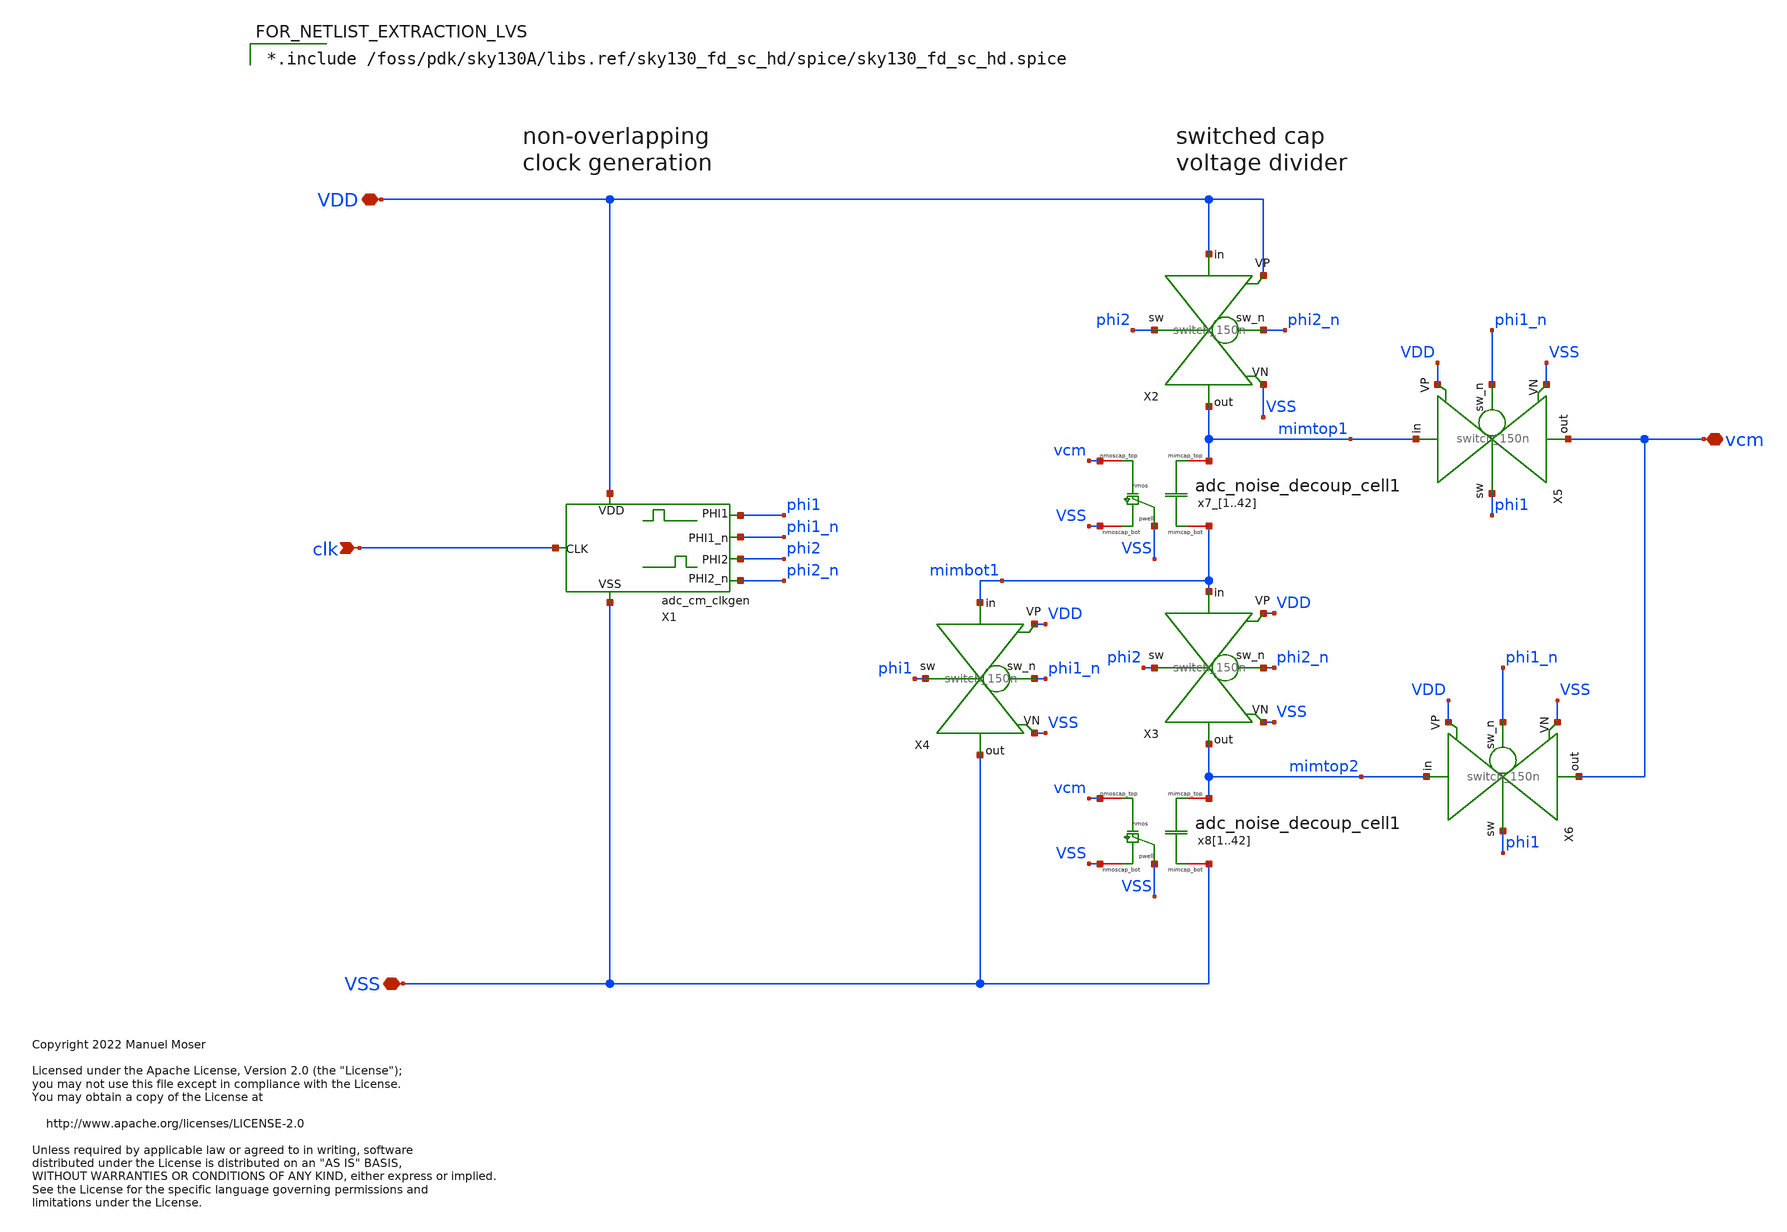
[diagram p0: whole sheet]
** sch_path: xschem/adc_vcm_gen/adc_vcm_gen.sch
* Copyright 2022 Manuel Moser
* Licensed under the Apache License, Version 2.0 (the "License");
**.subckt adc_vcm_gen VDD VSS clk vcm
*.iopin VDD
*.iopin VSS
*.ipin clk
*.iopin vcm
X1 clk VDD VSS phi1_n phi1 phi2 phi2_n adc_cm_clkgen
X2 phi2_n VDD phi2 mimtop1 VDD VSS switch_150n
X3 phi2_n mimbot1 phi2 mimtop2 VDD VSS switch_150n
X4 phi1_n mimbot1 phi1 VSS VDD VSS switch_150n
X5 phi1_n mimtop1 phi1 vcm VDD VSS switch_150n
X6 phi1_n mimtop2 phi1 vcm VDD VSS switch_150n
x7_1 mimtop1 mimbot1 vcm VSS VSS adc_noise_decoup_cell1
x7_2 mimtop1 mimbot1 vcm VSS VSS adc_noise_decoup_cell1
x7_3 mimtop1 mimbot1 vcm VSS VSS adc_noise_decoup_cell1
x7_4 mimtop1 mimbot1 vcm VSS VSS adc_noise_decoup_cell1
x7_5 mimtop1 mimbot1 vcm VSS VSS adc_noise_decoup_cell1
x7_6 mimtop1 mimbot1 vcm VSS VSS adc_noise_decoup_cell1
x7_7 mimtop1 mimbot1 vcm VSS VSS adc_noise_decoup_cell1
x7_8 mimtop1 mimbot1 vcm VSS VSS adc_noise_decoup_cell1
x7_9 mimtop1 mimbot1 vcm VSS VSS adc_noise_decoup_cell1
x7_10 mimtop1 mimbot1 vcm VSS VSS adc_noise_decoup_cell1
x7_11 mimtop1 mimbot1 vcm VSS VSS adc_noise_decoup_cell1
x7_12 mimtop1 mimbot1 vcm VSS VSS adc_noise_decoup_cell1
x7_13 mimtop1 mimbot1 vcm VSS VSS adc_noise_decoup_cell1
x7_14 mimtop1 mimbot1 vcm VSS VSS adc_noise_decoup_cell1
x7_15 mimtop1 mimbot1 vcm VSS VSS adc_noise_decoup_cell1
x7_16 mimtop1 mimbot1 vcm VSS VSS adc_noise_decoup_cell1
x7_17 mimtop1 mimbot1 vcm VSS VSS adc_noise_decoup_cell1
x7_18 mimtop1 mimbot1 vcm VSS VSS adc_noise_decoup_cell1
x7_19 mimtop1 mimbot1 vcm VSS VSS adc_noise_decoup_cell1
x7_20 mimtop1 mimbot1 vcm VSS VSS adc_noise_decoup_cell1
x7_21 mimtop1 mimbot1 vcm VSS VSS adc_noise_decoup_cell1
x7_22 mimtop1 mimbot1 vcm VSS VSS adc_noise_decoup_cell1
x7_23 mimtop1 mimbot1 vcm VSS VSS adc_noise_decoup_cell1
x7_24 mimtop1 mimbot1 vcm VSS VSS adc_noise_decoup_cell1
x7_25 mimtop1 mimbot1 vcm VSS VSS adc_noise_decoup_cell1
x7_26 mimtop1 mimbot1 vcm VSS VSS adc_noise_decoup_cell1
x7_27 mimtop1 mimbot1 vcm VSS VSS adc_noise_decoup_cell1
x7_28 mimtop1 mimbot1 vcm VSS VSS adc_noise_decoup_cell1
x7_29 mimtop1 mimbot1 vcm VSS VSS adc_noise_decoup_cell1
x7_30 mimtop1 mimbot1 vcm VSS VSS adc_noise_decoup_cell1
x7_31 mimtop1 mimbot1 vcm VSS VSS adc_noise_decoup_cell1
x7_32 mimtop1 mimbot1 vcm VSS VSS adc_noise_decoup_cell1
x7_33 mimtop1 mimbot1 vcm VSS VSS adc_noise_decoup_cell1
x7_34 mimtop1 mimbot1 vcm VSS VSS adc_noise_decoup_cell1
x7_35 mimtop1 mimbot1 vcm VSS VSS adc_noise_decoup_cell1
x7_36 mimtop1 mimbot1 vcm VSS VSS adc_noise_decoup_cell1
x7_37 mimtop1 mimbot1 vcm VSS VSS adc_noise_decoup_cell1
x7_38 mimtop1 mimbot1 vcm VSS VSS adc_noise_decoup_cell1
x7_39 mimtop1 mimbot1 vcm VSS VSS adc_noise_decoup_cell1
x7_40 mimtop1 mimbot1 vcm VSS VSS adc_noise_decoup_cell1
x7_41 mimtop1 mimbot1 vcm VSS VSS adc_noise_decoup_cell1
x7_42 mimtop1 mimbot1 vcm VSS VSS adc_noise_decoup_cell1
x81 mimtop2 VSS vcm VSS VSS adc_noise_decoup_cell1
x82 mimtop2 VSS vcm VSS VSS adc_noise_decoup_cell1
x83 mimtop2 VSS vcm VSS VSS adc_noise_decoup_cell1
x84 mimtop2 VSS vcm VSS VSS adc_noise_decoup_cell1
x85 mimtop2 VSS vcm VSS VSS adc_noise_decoup_cell1
x86 mimtop2 VSS vcm VSS VSS adc_noise_decoup_cell1
x87 mimtop2 VSS vcm VSS VSS adc_noise_decoup_cell1
x88 mimtop2 VSS vcm VSS VSS adc_noise_decoup_cell1
x89 mimtop2 VSS vcm VSS VSS adc_noise_decoup_cell1
x810 mimtop2 VSS vcm VSS VSS adc_noise_decoup_cell1
x811 mimtop2 VSS vcm VSS VSS adc_noise_decoup_cell1
x812 mimtop2 VSS vcm VSS VSS adc_noise_decoup_cell1
x813 mimtop2 VSS vcm VSS VSS adc_noise_decoup_cell1
x814 mimtop2 VSS vcm VSS VSS adc_noise_decoup_cell1
x815 mimtop2 VSS vcm VSS VSS adc_noise_decoup_cell1
x816 mimtop2 VSS vcm VSS VSS adc_noise_decoup_cell1
x817 mimtop2 VSS vcm VSS VSS adc_noise_decoup_cell1
x818 mimtop2 VSS vcm VSS VSS adc_noise_decoup_cell1
x819 mimtop2 VSS vcm VSS VSS adc_noise_decoup_cell1
x820 mimtop2 VSS vcm VSS VSS adc_noise_decoup_cell1
x821 mimtop2 VSS vcm VSS VSS adc_noise_decoup_cell1
x822 mimtop2 VSS vcm VSS VSS adc_noise_decoup_cell1
x823 mimtop2 VSS vcm VSS VSS adc_noise_decoup_cell1
x824 mimtop2 VSS vcm VSS VSS adc_noise_decoup_cell1
x825 mimtop2 VSS vcm VSS VSS adc_noise_decoup_cell1
x826 mimtop2 VSS vcm VSS VSS adc_noise_decoup_cell1
x827 mimtop2 VSS vcm VSS VSS adc_noise_decoup_cell1
x828 mimtop2 VSS vcm VSS VSS adc_noise_decoup_cell1
x829 mimtop2 VSS vcm VSS VSS adc_noise_decoup_cell1
x830 mimtop2 VSS vcm VSS VSS adc_noise_decoup_cell1
x831 mimtop2 VSS vcm VSS VSS adc_noise_decoup_cell1
x832 mimtop2 VSS vcm VSS VSS adc_noise_decoup_cell1
x833 mimtop2 VSS vcm VSS VSS adc_noise_decoup_cell1
x834 mimtop2 VSS vcm VSS VSS adc_noise_decoup_cell1
x835 mimtop2 VSS vcm VSS VSS adc_noise_decoup_cell1
x836 mimtop2 VSS vcm VSS VSS adc_noise_decoup_cell1
x837 mimtop2 VSS vcm VSS VSS adc_noise_decoup_cell1
x838 mimtop2 VSS vcm VSS VSS adc_noise_decoup_cell1
x839 mimtop2 VSS vcm VSS VSS adc_noise_decoup_cell1
x840 mimtop2 VSS vcm VSS VSS adc_noise_decoup_cell1
x841 mimtop2 VSS vcm VSS VSS adc_noise_decoup_cell1
x842 mimtop2 VSS vcm VSS VSS adc_noise_decoup_cell1
**** begin user architecture code

*.include /foss/pdk/sky130A/libs.ref/sky130_fd_sc_hd/spice/sky130_fd_sc_hd.spice

**** end user architecture code
**.ends
.end
